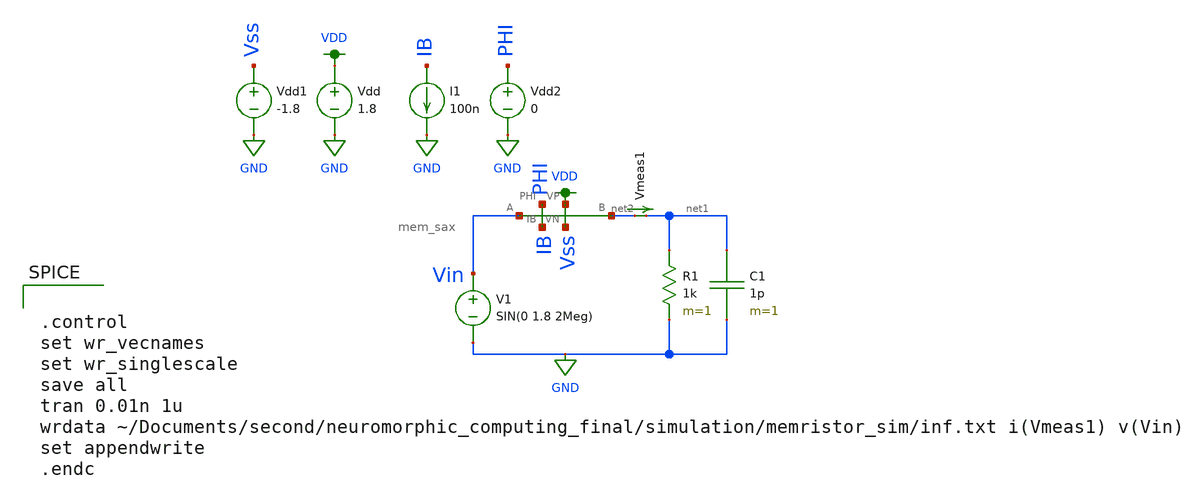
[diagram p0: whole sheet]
** sch_path: schematic/infinite_sax.sch
**.subckt infinite_sax
V1 Vin GND SIN(0 1.8 2Meg)
R1 net1 GND 1k m=1
C1 net1 GND 1p m=1
Vdd VDD GND 1.8
Vmeas1 net2 net1 0
.save i(vmeas1)
Vdd1 Vss GND -1.8
I1 IB GND 100n
Vdd2 PHI GND 0
X1 VDD Vss net2 Vin PHI IB mem_sax
**** begin user architecture code


.control
set wr_vecnames
set wr_singlescale
save all
tran 0.01n 1u
wrdata ~/Documents/second/neuromorphic_computing_final/simulation/memristor_sim/inf.txt i(Vmeas1)
+ v(Vin)
set appendwrite
.endc



.option wnflag=1
.param MC_SWITCH=1.0
.lib ~/skywater/skywater-pdk/libraries/sky130_fd_pr_ngspice/latest/models/sky130.lib.spice tt

**** end user architecture code
**.ends

* expanding   symbol:
*+  /home/madvlsi/Documents/second/neuromorphic_computing_final/schematic/mem_sax.sym # of pins=6
** sym_path: schematic/mem_sax.sym
** sch_path: schematic/mem_sax.sch
.subckt mem_sax VP VN B A PHI IB
*.ipin A
*.opin B
*.ipin PHI
*.iopin VP
*.iopin IB
*.iopin VN
XM1 VP net1 net2 VDD sky130_fd_pr__pfet_01v8 L=0.15 W=1 nf=1 ad='int((nf+1)/2) * W/nf * 0.29' as='int((nf+2)/2) * W/nf * 0.29'
+ pd='2*int((nf+1)/2) * (W/nf + 0.29)' ps='2*int((nf+2)/2) * (W/nf + 0.29)' nrd='0.29 / W' nrs='0.29 / W'
+ sa=0 sb=0 sd=0 mult=10 m=10
XM2 net1 net1 VP VDD sky130_fd_pr__pfet_01v8 L=0.15 W=1 nf=1 ad='int((nf+1)/2) * W/nf * 0.29' as='int((nf+2)/2) * W/nf * 0.29'
+ pd='2*int((nf+1)/2) * (W/nf + 0.29)' ps='2*int((nf+2)/2) * (W/nf + 0.29)' nrd='0.29 / W' nrs='0.29 / W'
+ sa=0 sb=0 sd=0 mult=10 m=10
XM3 net2 B IB GND sky130_fd_pr__nfet_01v8 L=0.15 W=1 nf=1 ad='int((nf+1)/2) * W/nf * 0.29' as='int((nf+2)/2) * W/nf * 0.29'
+ pd='2*int((nf+1)/2) * (W/nf + 0.29)' ps='2*int((nf+2)/2) * (W/nf + 0.29)' nrd='0.29 / W' nrs='0.29 / W'
+ sa=0 sb=0 sd=0 mult=1.3 m=1.3
XM4 IB A net1 GND sky130_fd_pr__nfet_01v8 L=0.15 W=1 nf=1 ad='int((nf+1)/2) * W/nf * 0.29' as='int((nf+2)/2) * W/nf * 0.29'
+ pd='2*int((nf+1)/2) * (W/nf + 0.29)' ps='2*int((nf+2)/2) * (W/nf + 0.29)' nrd='0.29 / W' nrs='0.29 / W'
+ sa=0 sb=0 sd=0 mult=1.3 m=1.3
XM5 net2 PHI net3 GND sky130_fd_pr__nfet_01v8 L=0.15 W=1 nf=1 ad='int((nf+1)/2) * W/nf * 0.29' as='int((nf+2)/2) * W/nf * 0.29'
+ pd='2*int((nf+1)/2) * (W/nf + 0.29)' ps='2*int((nf+2)/2) * (W/nf + 0.29)' nrd='0.29 / W' nrs='0.29 / W'
+ sa=0 sb=0 sd=0 mult=10 m=10
XM6 B net3 A GND sky130_fd_pr__nfet_01v8 L=0.15 W=1 nf=1 ad='int((nf+1)/2) * W/nf * 0.29' as='int((nf+2)/2) * W/nf * 0.29'
+ pd='2*int((nf+1)/2) * (W/nf + 0.29)' ps='2*int((nf+2)/2) * (W/nf + 0.29)' nrd='0.29 / W' nrs='0.29 / W'
+ sa=0 sb=0 sd=0 mult=7 m=7
C1 net3 VN 100f m=1
.ends

.GLOBAL VDD
.GLOBAL GND
.end
